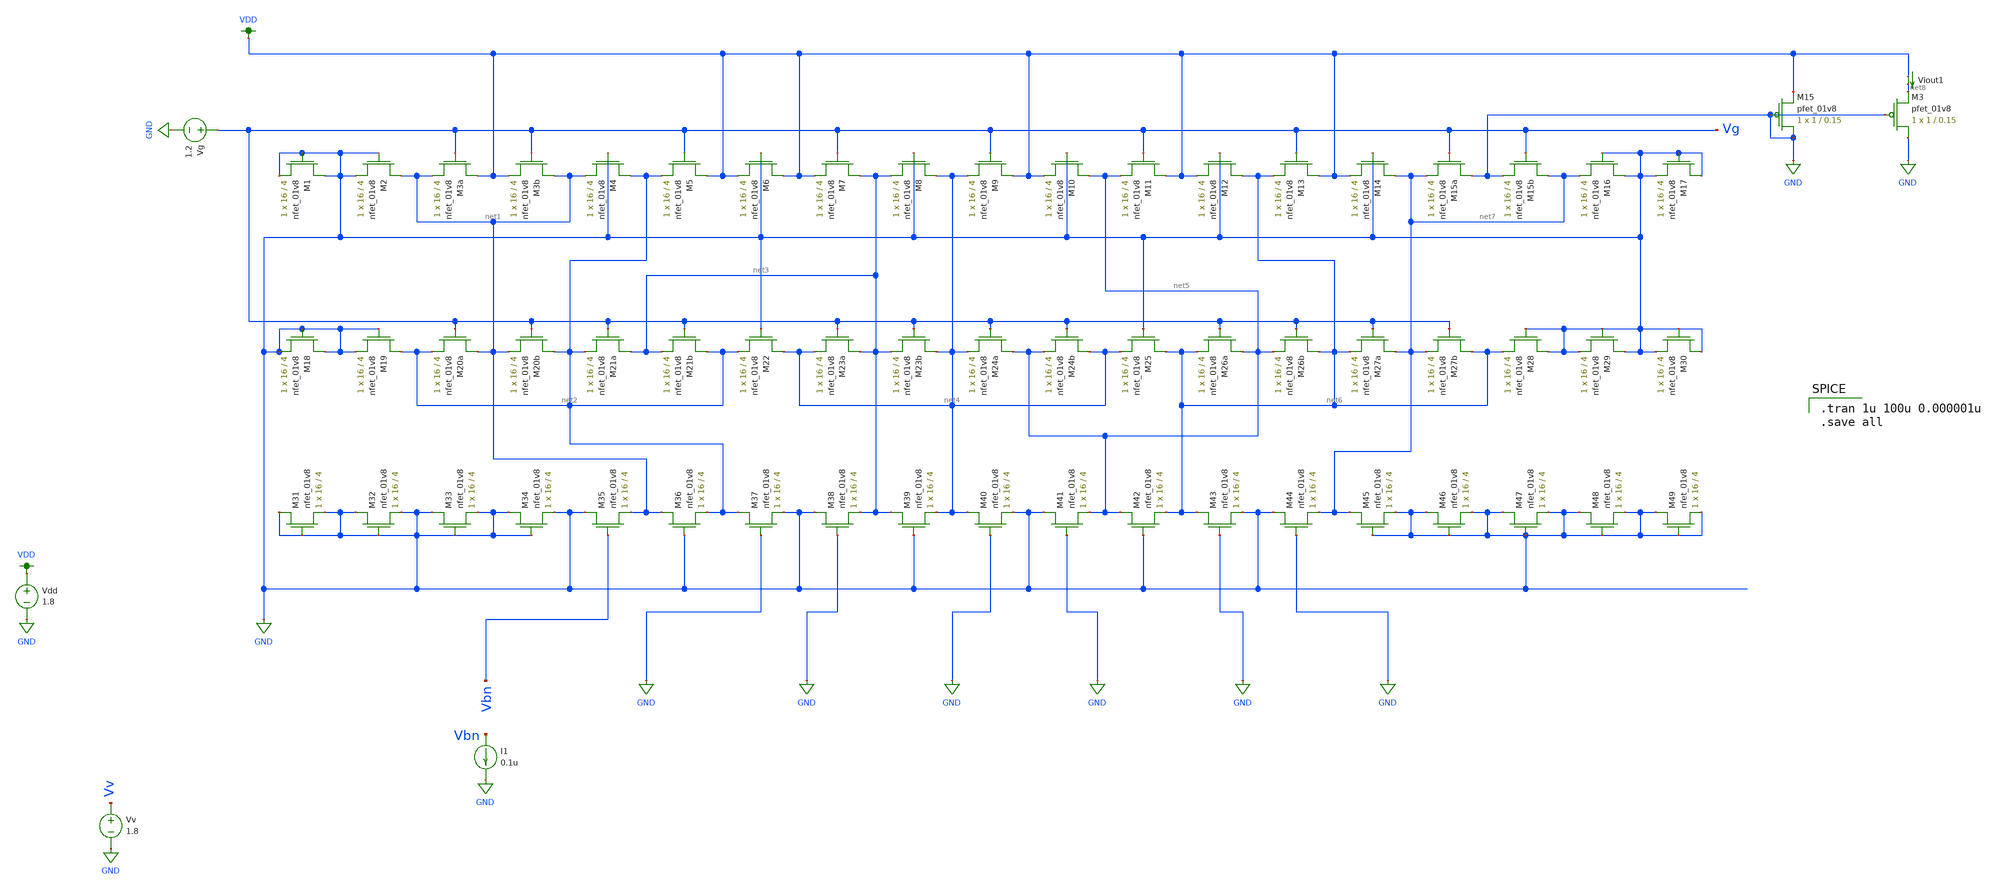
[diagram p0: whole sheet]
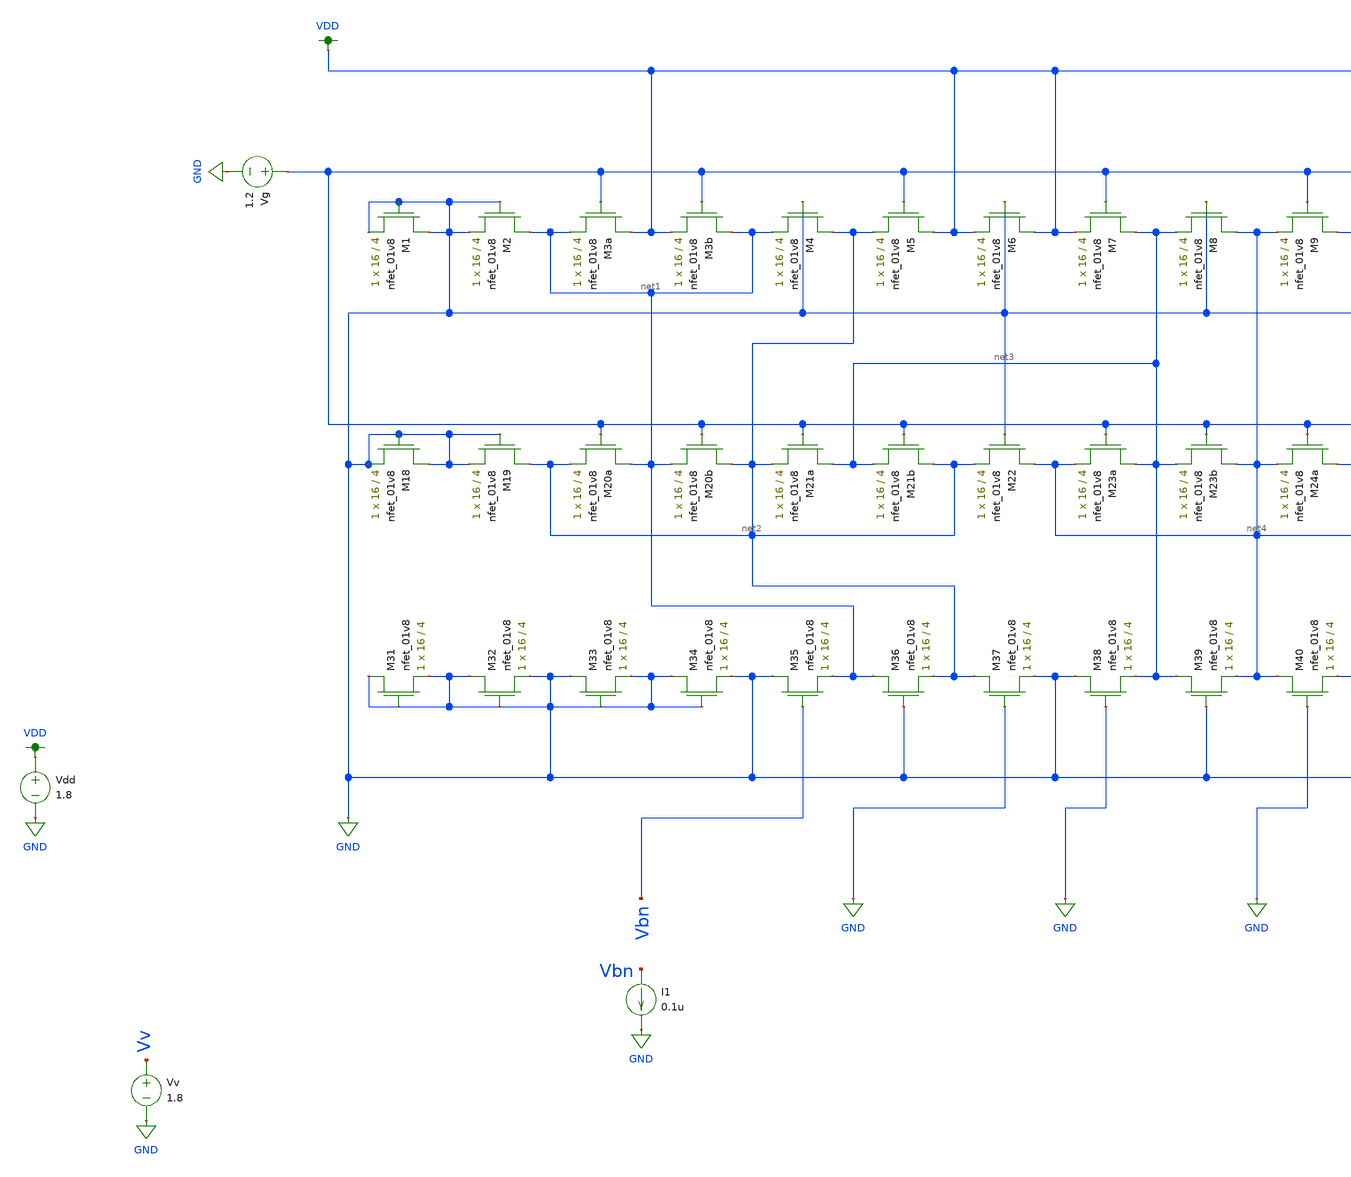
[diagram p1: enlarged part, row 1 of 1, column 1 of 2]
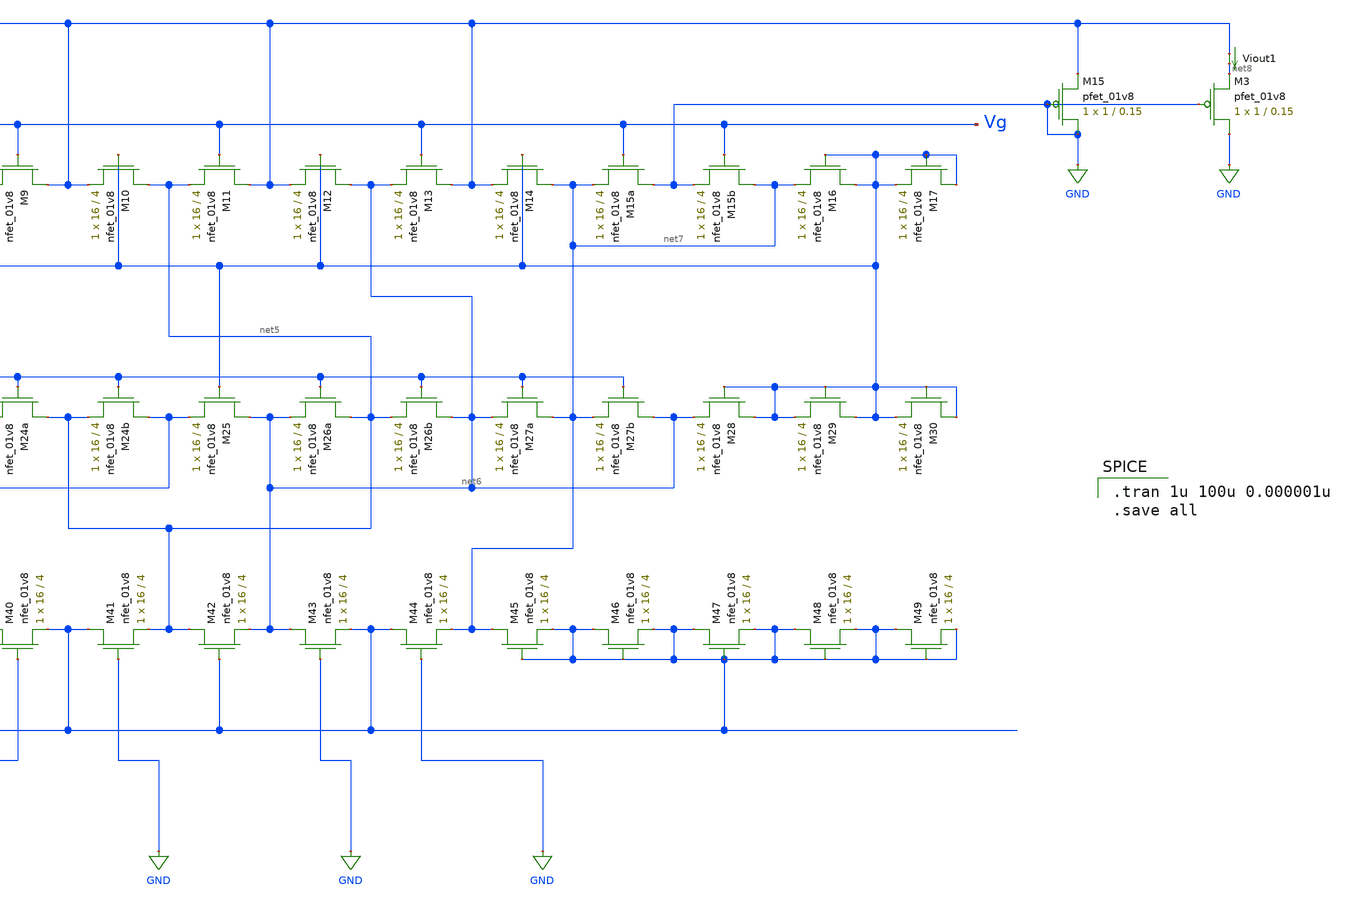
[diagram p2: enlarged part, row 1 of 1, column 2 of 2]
** sch_path: schematic/LDS/test/ladder_test.sch
**.subckt ladder_test
XM3a VDD Vg net1 GND sky130_fd_pr__nfet_01v8 L=4 W=16 nf=1 ad='int((nf+1)/2) * W/nf * 0.29' as='int((nf+2)/2) * W/nf * 0.29'
+ pd='2*int((nf+1)/2) * (W/nf + 0.29)' ps='2*int((nf+2)/2) * (W/nf + 0.29)' nrd='0.29 / W' nrs='0.29 / W'
+ sa=0 sb=0 sd=0 mult=1 m=1
XM3b net1 Vg VDD GND sky130_fd_pr__nfet_01v8 L=4 W=16 nf=1 ad='int((nf+1)/2) * W/nf * 0.29' as='int((nf+2)/2) * W/nf * 0.29'
+ pd='2*int((nf+1)/2) * (W/nf + 0.29)' ps='2*int((nf+2)/2) * (W/nf + 0.29)' nrd='0.29 / W' nrs='0.29 / W'
+ sa=0 sb=0 sd=0 mult=1 m=1
XM4 net2 GND net1 GND sky130_fd_pr__nfet_01v8 L=4 W=16 nf=1 ad='int((nf+1)/2) * W/nf * 0.29' as='int((nf+2)/2) * W/nf * 0.29'
+ pd='2*int((nf+1)/2) * (W/nf + 0.29)' ps='2*int((nf+2)/2) * (W/nf + 0.29)' nrd='0.29 / W' nrs='0.29 / W'
+ sa=0 sb=0 sd=0 mult=1 m=1
XM5 VDD Vg net2 GND sky130_fd_pr__nfet_01v8 L=4 W=16 nf=1 ad='int((nf+1)/2) * W/nf * 0.29' as='int((nf+2)/2) * W/nf * 0.29'
+ pd='2*int((nf+1)/2) * (W/nf + 0.29)' ps='2*int((nf+2)/2) * (W/nf + 0.29)' nrd='0.29 / W' nrs='0.29 / W'
+ sa=0 sb=0 sd=0 mult=1 m=1
XM6 VDD GND VDD GND sky130_fd_pr__nfet_01v8 L=4 W=16 nf=1 ad='int((nf+1)/2) * W/nf * 0.29' as='int((nf+2)/2) * W/nf * 0.29'
+ pd='2*int((nf+1)/2) * (W/nf + 0.29)' ps='2*int((nf+2)/2) * (W/nf + 0.29)' nrd='0.29 / W' nrs='0.29 / W'
+ sa=0 sb=0 sd=0 mult=1 m=1
XM7 net3 Vg VDD GND sky130_fd_pr__nfet_01v8 L=4 W=16 nf=1 ad='int((nf+1)/2) * W/nf * 0.29' as='int((nf+2)/2) * W/nf * 0.29'
+ pd='2*int((nf+1)/2) * (W/nf + 0.29)' ps='2*int((nf+2)/2) * (W/nf + 0.29)' nrd='0.29 / W' nrs='0.29 / W'
+ sa=0 sb=0 sd=0 mult=1 m=1
XM8 net4 GND net3 GND sky130_fd_pr__nfet_01v8 L=4 W=16 nf=1 ad='int((nf+1)/2) * W/nf * 0.29' as='int((nf+2)/2) * W/nf * 0.29'
+ pd='2*int((nf+1)/2) * (W/nf + 0.29)' ps='2*int((nf+2)/2) * (W/nf + 0.29)' nrd='0.29 / W' nrs='0.29 / W'
+ sa=0 sb=0 sd=0 mult=1 m=1
XM9 VDD Vg net4 GND sky130_fd_pr__nfet_01v8 L=4 W=16 nf=1 ad='int((nf+1)/2) * W/nf * 0.29' as='int((nf+2)/2) * W/nf * 0.29'
+ pd='2*int((nf+1)/2) * (W/nf + 0.29)' ps='2*int((nf+2)/2) * (W/nf + 0.29)' nrd='0.29 / W' nrs='0.29 / W'
+ sa=0 sb=0 sd=0 mult=1 m=1
XM10 net5 GND VDD GND sky130_fd_pr__nfet_01v8 L=4 W=16 nf=1 ad='int((nf+1)/2) * W/nf * 0.29' as='int((nf+2)/2) * W/nf * 0.29'
+ pd='2*int((nf+1)/2) * (W/nf + 0.29)' ps='2*int((nf+2)/2) * (W/nf + 0.29)' nrd='0.29 / W' nrs='0.29 / W'
+ sa=0 sb=0 sd=0 mult=1 m=1
XM11 VDD Vg net5 GND sky130_fd_pr__nfet_01v8 L=4 W=16 nf=1 ad='int((nf+1)/2) * W/nf * 0.29' as='int((nf+2)/2) * W/nf * 0.29'
+ pd='2*int((nf+1)/2) * (W/nf + 0.29)' ps='2*int((nf+2)/2) * (W/nf + 0.29)' nrd='0.29 / W' nrs='0.29 / W'
+ sa=0 sb=0 sd=0 mult=1 m=1
XM12 net6 GND VDD GND sky130_fd_pr__nfet_01v8 L=4 W=16 nf=1 ad='int((nf+1)/2) * W/nf * 0.29' as='int((nf+2)/2) * W/nf * 0.29'
+ pd='2*int((nf+1)/2) * (W/nf + 0.29)' ps='2*int((nf+2)/2) * (W/nf + 0.29)' nrd='0.29 / W' nrs='0.29 / W'
+ sa=0 sb=0 sd=0 mult=1 m=1
XM13 VDD Vg net6 GND sky130_fd_pr__nfet_01v8 L=4 W=16 nf=1 ad='int((nf+1)/2) * W/nf * 0.29' as='int((nf+2)/2) * W/nf * 0.29'
+ pd='2*int((nf+1)/2) * (W/nf + 0.29)' ps='2*int((nf+2)/2) * (W/nf + 0.29)' nrd='0.29 / W' nrs='0.29 / W'
+ sa=0 sb=0 sd=0 mult=1 m=1
XM14 net7 GND VDD GND sky130_fd_pr__nfet_01v8 L=4 W=16 nf=1 ad='int((nf+1)/2) * W/nf * 0.29' as='int((nf+2)/2) * W/nf * 0.29'
+ pd='2*int((nf+1)/2) * (W/nf + 0.29)' ps='2*int((nf+2)/2) * (W/nf + 0.29)' nrd='0.29 / W' nrs='0.29 / W'
+ sa=0 sb=0 sd=0 mult=1 m=1
XM15a GND Vg net7 GND sky130_fd_pr__nfet_01v8 L=4 W=16 nf=1 ad='int((nf+1)/2) * W/nf * 0.29' as='int((nf+2)/2) * W/nf * 0.29'
+ pd='2*int((nf+1)/2) * (W/nf + 0.29)' ps='2*int((nf+2)/2) * (W/nf + 0.29)' nrd='0.29 / W' nrs='0.29 / W'
+ sa=0 sb=0 sd=0 mult=1 m=1
XM15b net7 Vg GND GND sky130_fd_pr__nfet_01v8 L=4 W=16 nf=1 ad='int((nf+1)/2) * W/nf * 0.29' as='int((nf+2)/2) * W/nf * 0.29'
+ pd='2*int((nf+1)/2) * (W/nf + 0.29)' ps='2*int((nf+2)/2) * (W/nf + 0.29)' nrd='0.29 / W' nrs='0.29 / W'
+ sa=0 sb=0 sd=0 mult=1 m=1
XM20a net1 Vg net2 GND sky130_fd_pr__nfet_01v8 L=4 W=16 nf=1 ad='int((nf+1)/2) * W/nf * 0.29' as='int((nf+2)/2) * W/nf * 0.29'
+ pd='2*int((nf+1)/2) * (W/nf + 0.29)' ps='2*int((nf+2)/2) * (W/nf + 0.29)' nrd='0.29 / W' nrs='0.29 / W'
+ sa=0 sb=0 sd=0 mult=1 m=1
XM20b net2 Vg net1 GND sky130_fd_pr__nfet_01v8 L=4 W=16 nf=1 ad='int((nf+1)/2) * W/nf * 0.29' as='int((nf+2)/2) * W/nf * 0.29'
+ pd='2*int((nf+1)/2) * (W/nf + 0.29)' ps='2*int((nf+2)/2) * (W/nf + 0.29)' nrd='0.29 / W' nrs='0.29 / W'
+ sa=0 sb=0 sd=0 mult=1 m=1
XM21a net3 Vg net2 GND sky130_fd_pr__nfet_01v8 L=4 W=16 nf=1 ad='int((nf+1)/2) * W/nf * 0.29' as='int((nf+2)/2) * W/nf * 0.29'
+ pd='2*int((nf+1)/2) * (W/nf + 0.29)' ps='2*int((nf+2)/2) * (W/nf + 0.29)' nrd='0.29 / W' nrs='0.29 / W'
+ sa=0 sb=0 sd=0 mult=1 m=1
XM21b net2 Vg net3 GND sky130_fd_pr__nfet_01v8 L=4 W=16 nf=1 ad='int((nf+1)/2) * W/nf * 0.29' as='int((nf+2)/2) * W/nf * 0.29'
+ pd='2*int((nf+1)/2) * (W/nf + 0.29)' ps='2*int((nf+2)/2) * (W/nf + 0.29)' nrd='0.29 / W' nrs='0.29 / W'
+ sa=0 sb=0 sd=0 mult=1 m=1
XM22 net4 GND net2 GND sky130_fd_pr__nfet_01v8 L=4 W=16 nf=1 ad='int((nf+1)/2) * W/nf * 0.29' as='int((nf+2)/2) * W/nf * 0.29'
+ pd='2*int((nf+1)/2) * (W/nf + 0.29)' ps='2*int((nf+2)/2) * (W/nf + 0.29)' nrd='0.29 / W' nrs='0.29 / W'
+ sa=0 sb=0 sd=0 mult=1 m=1
XM23a net3 Vg net4 GND sky130_fd_pr__nfet_01v8 L=4 W=16 nf=1 ad='int((nf+1)/2) * W/nf * 0.29' as='int((nf+2)/2) * W/nf * 0.29'
+ pd='2*int((nf+1)/2) * (W/nf + 0.29)' ps='2*int((nf+2)/2) * (W/nf + 0.29)' nrd='0.29 / W' nrs='0.29 / W'
+ sa=0 sb=0 sd=0 mult=1 m=1
XM23b net4 Vg net3 GND sky130_fd_pr__nfet_01v8 L=4 W=16 nf=1 ad='int((nf+1)/2) * W/nf * 0.29' as='int((nf+2)/2) * W/nf * 0.29'
+ pd='2*int((nf+1)/2) * (W/nf + 0.29)' ps='2*int((nf+2)/2) * (W/nf + 0.29)' nrd='0.29 / W' nrs='0.29 / W'
+ sa=0 sb=0 sd=0 mult=1 m=1
XM24a net5 Vg net4 GND sky130_fd_pr__nfet_01v8 L=4 W=16 nf=1 ad='int((nf+1)/2) * W/nf * 0.29' as='int((nf+2)/2) * W/nf * 0.29'
+ pd='2*int((nf+1)/2) * (W/nf + 0.29)' ps='2*int((nf+2)/2) * (W/nf + 0.29)' nrd='0.29 / W' nrs='0.29 / W'
+ sa=0 sb=0 sd=0 mult=1 m=1
XM24b net4 Vg net5 GND sky130_fd_pr__nfet_01v8 L=4 W=16 nf=1 ad='int((nf+1)/2) * W/nf * 0.29' as='int((nf+2)/2) * W/nf * 0.29'
+ pd='2*int((nf+1)/2) * (W/nf + 0.29)' ps='2*int((nf+2)/2) * (W/nf + 0.29)' nrd='0.29 / W' nrs='0.29 / W'
+ sa=0 sb=0 sd=0 mult=1 m=1
XM25 net6 GND net4 GND sky130_fd_pr__nfet_01v8 L=4 W=16 nf=1 ad='int((nf+1)/2) * W/nf * 0.29' as='int((nf+2)/2) * W/nf * 0.29'
+ pd='2*int((nf+1)/2) * (W/nf + 0.29)' ps='2*int((nf+2)/2) * (W/nf + 0.29)' nrd='0.29 / W' nrs='0.29 / W'
+ sa=0 sb=0 sd=0 mult=1 m=1
XM26a net5 Vg net6 GND sky130_fd_pr__nfet_01v8 L=4 W=16 nf=1 ad='int((nf+1)/2) * W/nf * 0.29' as='int((nf+2)/2) * W/nf * 0.29'
+ pd='2*int((nf+1)/2) * (W/nf + 0.29)' ps='2*int((nf+2)/2) * (W/nf + 0.29)' nrd='0.29 / W' nrs='0.29 / W'
+ sa=0 sb=0 sd=0 mult=1 m=1
XM26b net6 Vg net5 GND sky130_fd_pr__nfet_01v8 L=4 W=16 nf=1 ad='int((nf+1)/2) * W/nf * 0.29' as='int((nf+2)/2) * W/nf * 0.29'
+ pd='2*int((nf+1)/2) * (W/nf + 0.29)' ps='2*int((nf+2)/2) * (W/nf + 0.29)' nrd='0.29 / W' nrs='0.29 / W'
+ sa=0 sb=0 sd=0 mult=1 m=1
XM27a net7 Vg net6 GND sky130_fd_pr__nfet_01v8 L=4 W=16 nf=1 ad='int((nf+1)/2) * W/nf * 0.29' as='int((nf+2)/2) * W/nf * 0.29'
+ pd='2*int((nf+1)/2) * (W/nf + 0.29)' ps='2*int((nf+2)/2) * (W/nf + 0.29)' nrd='0.29 / W' nrs='0.29 / W'
+ sa=0 sb=0 sd=0 mult=1 m=1
XM27b net6 Vg net7 GND sky130_fd_pr__nfet_01v8 L=4 W=16 nf=1 ad='int((nf+1)/2) * W/nf * 0.29' as='int((nf+2)/2) * W/nf * 0.29'
+ pd='2*int((nf+1)/2) * (W/nf + 0.29)' ps='2*int((nf+2)/2) * (W/nf + 0.29)' nrd='0.29 / W' nrs='0.29 / W'
+ sa=0 sb=0 sd=0 mult=1 m=1
XM35 GND Vbn net1 GND sky130_fd_pr__nfet_01v8 L=4 W=16 nf=1 ad='int((nf+1)/2) * W/nf * 0.29' as='int((nf+2)/2) * W/nf * 0.29'
+ pd='2*int((nf+1)/2) * (W/nf + 0.29)' ps='2*int((nf+2)/2) * (W/nf + 0.29)' nrd='0.29 / W' nrs='0.29 / W'
+ sa=0 sb=0 sd=0 mult=1 m=1
XM36 net1 GND net2 GND sky130_fd_pr__nfet_01v8 L=4 W=16 nf=1 ad='int((nf+1)/2) * W/nf * 0.29' as='int((nf+2)/2) * W/nf * 0.29'
+ pd='2*int((nf+1)/2) * (W/nf + 0.29)' ps='2*int((nf+2)/2) * (W/nf + 0.29)' nrd='0.29 / W' nrs='0.29 / W'
+ sa=0 sb=0 sd=0 mult=1 m=1
XM37 net2 GND GND GND sky130_fd_pr__nfet_01v8 L=4 W=16 nf=1 ad='int((nf+1)/2) * W/nf * 0.29' as='int((nf+2)/2) * W/nf * 0.29'
+ pd='2*int((nf+1)/2) * (W/nf + 0.29)' ps='2*int((nf+2)/2) * (W/nf + 0.29)' nrd='0.29 / W' nrs='0.29 / W'
+ sa=0 sb=0 sd=0 mult=1 m=1
XM38 GND GND net3 GND sky130_fd_pr__nfet_01v8 L=4 W=16 nf=1 ad='int((nf+1)/2) * W/nf * 0.29' as='int((nf+2)/2) * W/nf * 0.29'
+ pd='2*int((nf+1)/2) * (W/nf + 0.29)' ps='2*int((nf+2)/2) * (W/nf + 0.29)' nrd='0.29 / W' nrs='0.29 / W'
+ sa=0 sb=0 sd=0 mult=1 m=1
XM39 net3 GND net4 GND sky130_fd_pr__nfet_01v8 L=4 W=16 nf=1 ad='int((nf+1)/2) * W/nf * 0.29' as='int((nf+2)/2) * W/nf * 0.29'
+ pd='2*int((nf+1)/2) * (W/nf + 0.29)' ps='2*int((nf+2)/2) * (W/nf + 0.29)' nrd='0.29 / W' nrs='0.29 / W'
+ sa=0 sb=0 sd=0 mult=1 m=1
XM40 net4 GND GND GND sky130_fd_pr__nfet_01v8 L=4 W=16 nf=1 ad='int((nf+1)/2) * W/nf * 0.29' as='int((nf+2)/2) * W/nf * 0.29'
+ pd='2*int((nf+1)/2) * (W/nf + 0.29)' ps='2*int((nf+2)/2) * (W/nf + 0.29)' nrd='0.29 / W' nrs='0.29 / W'
+ sa=0 sb=0 sd=0 mult=1 m=1
XM41 GND GND net5 GND sky130_fd_pr__nfet_01v8 L=4 W=16 nf=1 ad='int((nf+1)/2) * W/nf * 0.29' as='int((nf+2)/2) * W/nf * 0.29'
+ pd='2*int((nf+1)/2) * (W/nf + 0.29)' ps='2*int((nf+2)/2) * (W/nf + 0.29)' nrd='0.29 / W' nrs='0.29 / W'
+ sa=0 sb=0 sd=0 mult=1 m=1
XM42 net5 GND net6 GND sky130_fd_pr__nfet_01v8 L=4 W=16 nf=1 ad='int((nf+1)/2) * W/nf * 0.29' as='int((nf+2)/2) * W/nf * 0.29'
+ pd='2*int((nf+1)/2) * (W/nf + 0.29)' ps='2*int((nf+2)/2) * (W/nf + 0.29)' nrd='0.29 / W' nrs='0.29 / W'
+ sa=0 sb=0 sd=0 mult=1 m=1
XM43 net6 GND GND GND sky130_fd_pr__nfet_01v8 L=4 W=16 nf=1 ad='int((nf+1)/2) * W/nf * 0.29' as='int((nf+2)/2) * W/nf * 0.29'
+ pd='2*int((nf+1)/2) * (W/nf + 0.29)' ps='2*int((nf+2)/2) * (W/nf + 0.29)' nrd='0.29 / W' nrs='0.29 / W'
+ sa=0 sb=0 sd=0 mult=1 m=1
XM44 GND GND net7 GND sky130_fd_pr__nfet_01v8 L=4 W=16 nf=1 ad='int((nf+1)/2) * W/nf * 0.29' as='int((nf+2)/2) * W/nf * 0.29'
+ pd='2*int((nf+1)/2) * (W/nf + 0.29)' ps='2*int((nf+2)/2) * (W/nf + 0.29)' nrd='0.29 / W' nrs='0.29 / W'
+ sa=0 sb=0 sd=0 mult=1 m=1
XM16 GND GND net7 GND sky130_fd_pr__nfet_01v8 L=4 W=16 nf=1 ad='int((nf+1)/2) * W/nf * 0.29' as='int((nf+2)/2) * W/nf * 0.29'
+ pd='2*int((nf+1)/2) * (W/nf + 0.29)' ps='2*int((nf+2)/2) * (W/nf + 0.29)' nrd='0.29 / W' nrs='0.29 / W'
+ sa=0 sb=0 sd=0 mult=1 m=1
XM17 GND GND GND GND sky130_fd_pr__nfet_01v8 L=4 W=16 nf=1 ad='int((nf+1)/2) * W/nf * 0.29' as='int((nf+2)/2) * W/nf * 0.29'
+ pd='2*int((nf+1)/2) * (W/nf + 0.29)' ps='2*int((nf+2)/2) * (W/nf + 0.29)' nrd='0.29 / W' nrs='0.29 / W'
+ sa=0 sb=0 sd=0 mult=1 m=1
XM2 net1 GND GND GND sky130_fd_pr__nfet_01v8 L=4 W=16 nf=1 ad='int((nf+1)/2) * W/nf * 0.29' as='int((nf+2)/2) * W/nf * 0.29'
+ pd='2*int((nf+1)/2) * (W/nf + 0.29)' ps='2*int((nf+2)/2) * (W/nf + 0.29)' nrd='0.29 / W' nrs='0.29 / W'
+ sa=0 sb=0 sd=0 mult=1 m=1
XM1 GND GND GND GND sky130_fd_pr__nfet_01v8 L=4 W=16 nf=1 ad='int((nf+1)/2) * W/nf * 0.29' as='int((nf+2)/2) * W/nf * 0.29'
+ pd='2*int((nf+1)/2) * (W/nf + 0.29)' ps='2*int((nf+2)/2) * (W/nf + 0.29)' nrd='0.29 / W' nrs='0.29 / W'
+ sa=0 sb=0 sd=0 mult=1 m=1
XM19 net2 GND GND GND sky130_fd_pr__nfet_01v8 L=4 W=16 nf=1 ad='int((nf+1)/2) * W/nf * 0.29' as='int((nf+2)/2) * W/nf * 0.29'
+ pd='2*int((nf+1)/2) * (W/nf + 0.29)' ps='2*int((nf+2)/2) * (W/nf + 0.29)' nrd='0.29 / W' nrs='0.29 / W'
+ sa=0 sb=0 sd=0 mult=1 m=1
XM18 GND GND GND GND sky130_fd_pr__nfet_01v8 L=4 W=16 nf=1 ad='int((nf+1)/2) * W/nf * 0.29' as='int((nf+2)/2) * W/nf * 0.29'
+ pd='2*int((nf+1)/2) * (W/nf + 0.29)' ps='2*int((nf+2)/2) * (W/nf + 0.29)' nrd='0.29 / W' nrs='0.29 / W'
+ sa=0 sb=0 sd=0 mult=1 m=1
XM28 GND GND net6 GND sky130_fd_pr__nfet_01v8 L=4 W=16 nf=1 ad='int((nf+1)/2) * W/nf * 0.29' as='int((nf+2)/2) * W/nf * 0.29'
+ pd='2*int((nf+1)/2) * (W/nf + 0.29)' ps='2*int((nf+2)/2) * (W/nf + 0.29)' nrd='0.29 / W' nrs='0.29 / W'
+ sa=0 sb=0 sd=0 mult=1 m=1
XM29 GND GND GND GND sky130_fd_pr__nfet_01v8 L=4 W=16 nf=1 ad='int((nf+1)/2) * W/nf * 0.29' as='int((nf+2)/2) * W/nf * 0.29'
+ pd='2*int((nf+1)/2) * (W/nf + 0.29)' ps='2*int((nf+2)/2) * (W/nf + 0.29)' nrd='0.29 / W' nrs='0.29 / W'
+ sa=0 sb=0 sd=0 mult=1 m=1
XM30 GND GND GND GND sky130_fd_pr__nfet_01v8 L=4 W=16 nf=1 ad='int((nf+1)/2) * W/nf * 0.29' as='int((nf+2)/2) * W/nf * 0.29'
+ pd='2*int((nf+1)/2) * (W/nf + 0.29)' ps='2*int((nf+2)/2) * (W/nf + 0.29)' nrd='0.29 / W' nrs='0.29 / W'
+ sa=0 sb=0 sd=0 mult=1 m=1
XM45 net7 GND GND GND sky130_fd_pr__nfet_01v8 L=4 W=16 nf=1 ad='int((nf+1)/2) * W/nf * 0.29' as='int((nf+2)/2) * W/nf * 0.29'
+ pd='2*int((nf+1)/2) * (W/nf + 0.29)' ps='2*int((nf+2)/2) * (W/nf + 0.29)' nrd='0.29 / W' nrs='0.29 / W'
+ sa=0 sb=0 sd=0 mult=1 m=1
XM46 GND GND GND GND sky130_fd_pr__nfet_01v8 L=4 W=16 nf=1 ad='int((nf+1)/2) * W/nf * 0.29' as='int((nf+2)/2) * W/nf * 0.29'
+ pd='2*int((nf+1)/2) * (W/nf + 0.29)' ps='2*int((nf+2)/2) * (W/nf + 0.29)' nrd='0.29 / W' nrs='0.29 / W'
+ sa=0 sb=0 sd=0 mult=1 m=1
XM47 GND GND GND GND sky130_fd_pr__nfet_01v8 L=4 W=16 nf=1 ad='int((nf+1)/2) * W/nf * 0.29' as='int((nf+2)/2) * W/nf * 0.29'
+ pd='2*int((nf+1)/2) * (W/nf + 0.29)' ps='2*int((nf+2)/2) * (W/nf + 0.29)' nrd='0.29 / W' nrs='0.29 / W'
+ sa=0 sb=0 sd=0 mult=1 m=1
XM48 GND GND GND GND sky130_fd_pr__nfet_01v8 L=4 W=16 nf=1 ad='int((nf+1)/2) * W/nf * 0.29' as='int((nf+2)/2) * W/nf * 0.29'
+ pd='2*int((nf+1)/2) * (W/nf + 0.29)' ps='2*int((nf+2)/2) * (W/nf + 0.29)' nrd='0.29 / W' nrs='0.29 / W'
+ sa=0 sb=0 sd=0 mult=1 m=1
XM49 GND GND GND GND sky130_fd_pr__nfet_01v8 L=4 W=16 nf=1 ad='int((nf+1)/2) * W/nf * 0.29' as='int((nf+2)/2) * W/nf * 0.29'
+ pd='2*int((nf+1)/2) * (W/nf + 0.29)' ps='2*int((nf+2)/2) * (W/nf + 0.29)' nrd='0.29 / W' nrs='0.29 / W'
+ sa=0 sb=0 sd=0 mult=1 m=1
XM34 GND GND GND GND sky130_fd_pr__nfet_01v8 L=4 W=16 nf=1 ad='int((nf+1)/2) * W/nf * 0.29' as='int((nf+2)/2) * W/nf * 0.29'
+ pd='2*int((nf+1)/2) * (W/nf + 0.29)' ps='2*int((nf+2)/2) * (W/nf + 0.29)' nrd='0.29 / W' nrs='0.29 / W'
+ sa=0 sb=0 sd=0 mult=1 m=1
XM33 GND GND GND GND sky130_fd_pr__nfet_01v8 L=4 W=16 nf=1 ad='int((nf+1)/2) * W/nf * 0.29' as='int((nf+2)/2) * W/nf * 0.29'
+ pd='2*int((nf+1)/2) * (W/nf + 0.29)' ps='2*int((nf+2)/2) * (W/nf + 0.29)' nrd='0.29 / W' nrs='0.29 / W'
+ sa=0 sb=0 sd=0 mult=1 m=1
XM32 GND GND GND GND sky130_fd_pr__nfet_01v8 L=4 W=16 nf=1 ad='int((nf+1)/2) * W/nf * 0.29' as='int((nf+2)/2) * W/nf * 0.29'
+ pd='2*int((nf+1)/2) * (W/nf + 0.29)' ps='2*int((nf+2)/2) * (W/nf + 0.29)' nrd='0.29 / W' nrs='0.29 / W'
+ sa=0 sb=0 sd=0 mult=1 m=1
XM31 GND GND GND GND sky130_fd_pr__nfet_01v8 L=4 W=16 nf=1 ad='int((nf+1)/2) * W/nf * 0.29' as='int((nf+2)/2) * W/nf * 0.29'
+ pd='2*int((nf+1)/2) * (W/nf + 0.29)' ps='2*int((nf+2)/2) * (W/nf + 0.29)' nrd='0.29 / W' nrs='0.29 / W'
+ sa=0 sb=0 sd=0 mult=1 m=1
Vg Vg GND 1.2
XM3 GND GND net8 VDD sky130_fd_pr__pfet_01v8 L=0.15 W=1 nf=1 ad='int((nf+1)/2) * W/nf * 0.29' as='int((nf+2)/2) * W/nf * 0.29'
+ pd='2*int((nf+1)/2) * (W/nf + 0.29)' ps='2*int((nf+2)/2) * (W/nf + 0.29)' nrd='0.29 / W' nrs='0.29 / W'
+ sa=0 sb=0 sd=0 mult=1 m=1
XM15 GND GND VDD VDD sky130_fd_pr__pfet_01v8 L=0.15 W=1 nf=1 ad='int((nf+1)/2) * W/nf * 0.29' as='int((nf+2)/2) * W/nf * 0.29'
+ pd='2*int((nf+1)/2) * (W/nf + 0.29)' ps='2*int((nf+2)/2) * (W/nf + 0.29)' nrd='0.29 / W' nrs='0.29 / W'
+ sa=0 sb=0 sd=0 mult=1 m=1
Viout1 VDD net8 0
.save i(viout1)
Vdd VDD GND 1.8
I1 Vbn GND 0.1u
Vv Vv GND 1.8
**** begin user architecture code

.option wnflag=1
.param MC_SWITCH=0.0
.lib ~/skywater/skywater-pdk/libraries/sky130_fd_pr_ngspice/latest/models/sky130.lib.spice tt


.tran 1u 100u 0.000001u
.save all


**** end user architecture code
**.ends
.GLOBAL VDD
.GLOBAL GND
.end
